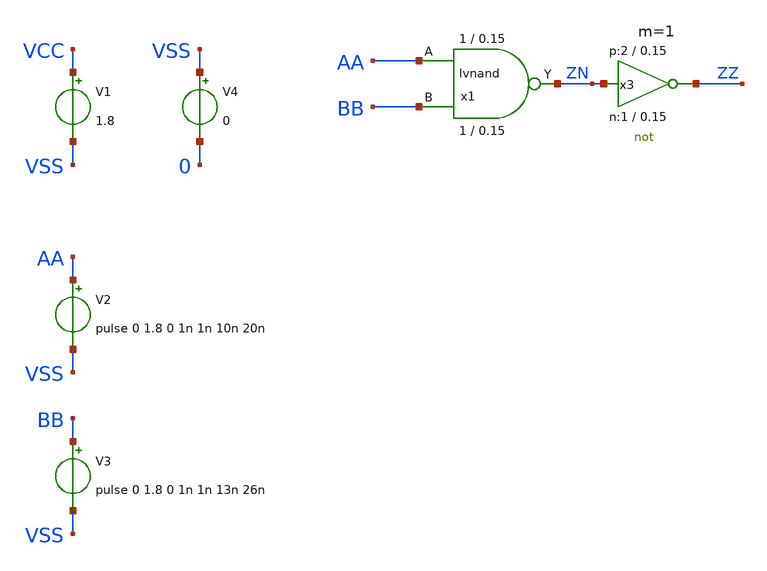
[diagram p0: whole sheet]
** sch_path: sky130_tests/logic_ngspice.sch
* Copyright 2021 Stefan Frederik Schippers
* Licensed under the Apache License, Version 2.0 (the "License");
* you may not use this file except in compliance with the License.
* You may obtain a copy of the License at
* https://www.apache.org/licenses/LICENSE-2.0
* Unless required by applicable law or agreed to in writing, software
* distributed under the License is distributed on an "AS IS" BASIS,
* WITHOUT WARRANTIES OR CONDITIONS OF ANY KIND, either express or implied.
* See the License for the specific language governing permissions and
* limitations under the License.
* sky130_tests/not.sym:
* Copyright 2020 Stefan Frederik Schippers
**.subckt logic_ngspice
x1 AA BB ZN lvnand WidthN=1 LenN=0.15 WidthP=1 LenP=0.15 m=1
V1 VCC VSS 1.8
V2 AA VSS pulse 0 1.8 0 1n 1n 10n 20n
V3 BB VSS pulse 0 1.8 0 1n 1n 13n 26n
x3 ZZ ZN VCC VSS not W_N=1 L_N=0.15 W_P=2 L_P=0.15 m=1
V4 VSS 0 0
**** begin user architecture code


.control
save all
tran 0.1n 200n
write logic_ngspice.raw
plot aa bb+2 zz+4
.endc



** opencircuitdesign pdks install
.lib $::SKYWATER_MODELS/sky130.lib.spice tt

**** end user architecture code
**.ends

* expanding   symbol:  sky130_tests/lvnand.sym # of pins=3
** sym_path: sky130_tests/lvnand.sym
** sch_path: sky130_tests/lvnand.sch
.subckt lvnand A B Y  WidthN=1 LenN=0.15 WidthP=1 LenP=0.15
*.ipin A
*.ipin B
*.opin Y
XM1 Y B S VSSPIN sky130_fd_pr__nfet_01v8 L=LenN W=WidthN nf=1 ad='int((1 + 1)/2) * WidthN / 1 * 0.29'
+ as='int((1 + 2)/2) * WidthN / 1 * 0.29' pd='2*int((1 + 1)/2) * (WidthN / 1 + 0.29)' ps='2*int((1 + 2)/2) * (WidthN / 1 + 0.29)'
+ nrd='0.29 / WidthN ' nrs='0.29 / WidthN ' sa=0 sb=0 sd=0 mult=1 m=1
XM2 Y A VCCPIN VCCPIN sky130_fd_pr__pfet_01v8 L=LenP W=WidthP nf=1 ad='int((1 + 1)/2) * WidthP / 1 * 0.29'
+ as='int((1 + 2)/2) * WidthP / 1 * 0.29' pd='2*int((1 + 1)/2) * (WidthP / 1 + 0.29)' ps='2*int((1 + 2)/2) * (WidthP / 1 + 0.29)'
+ nrd='0.29 / WidthP ' nrs='0.29 / WidthP ' sa=0 sb=0 sd=0 mult=1 m=1
XM3 Y B VCCPIN VCCPIN sky130_fd_pr__pfet_01v8 L=LenP W=WidthP nf=1 ad='int((1 + 1)/2) * WidthP / 1 * 0.29'
+ as='int((1 + 2)/2) * WidthP / 1 * 0.29' pd='2*int((1 + 1)/2) * (WidthP / 1 + 0.29)' ps='2*int((1 + 2)/2) * (WidthP / 1 + 0.29)'
+ nrd='0.29 / WidthP ' nrs='0.29 / WidthP ' sa=0 sb=0 sd=0 mult=1 m=1
XM4 S A VSSPIN VSSPIN sky130_fd_pr__nfet_01v8 L=LenN W=WidthN nf=1 ad='int((1 + 1)/2) * WidthN / 1 * 0.29'
+ as='int((1 + 2)/2) * WidthN / 1 * 0.29' pd='2*int((1 + 1)/2) * (WidthN / 1 + 0.29)' ps='2*int((1 + 2)/2) * (WidthN / 1 + 0.29)'
+ nrd='0.29 / WidthN ' nrs='0.29 / WidthN ' sa=0 sb=0 sd=0 mult=1 m=1
.ends


* expanding   symbol:  sky130_tests/not.sym # of pins=2
** sym_path: sky130_tests/not.sym
** sch_path: sky130_tests/not.sch
.subckt not y a VCCPIN VSSPIN     W_N=1 L_N=0.15 W_P=2 L_P=0.15
*.opin y
*.ipin a
XM1 DN a VSSPIN VSSPIN sky130_fd_pr__nfet_01v8 L=L_N W=W_N nf=1 ad='int((1 + 1)/2) * W_N / 1 * 0.29'
+ as='int((1 + 2)/2) * W_N / 1 * 0.29' pd='2*int((1 + 1)/2) * (W_N / 1 + 0.29)' ps='2*int((1 + 2)/2) * (W_N / 1 + 0.29)'
+ nrd='0.29 / W_N ' nrs='0.29 / W_N ' sa=0 sb=0 sd=0 mult=1 m=1
XM2 DP a VCCPIN VCCPIN sky130_fd_pr__pfet_01v8 L=L_P W=W_P nf=1 ad='int((1 + 1)/2) * W_P / 1 * 0.29'
+ as='int((1 + 2)/2) * W_P / 1 * 0.29' pd='2*int((1 + 1)/2) * (W_P / 1 + 0.29)' ps='2*int((1 + 2)/2) * (W_P / 1 + 0.29)'
+ nrd='0.29 / W_P ' nrs='0.29 / W_P ' sa=0 sb=0 sd=0 mult=1 m=1
Vmeas DP y 0
.save i(vmeas)
Vmeas1 y DN 0
.save i(vmeas1)
.save v(dp)
.save v(dn)
.ends

.end
